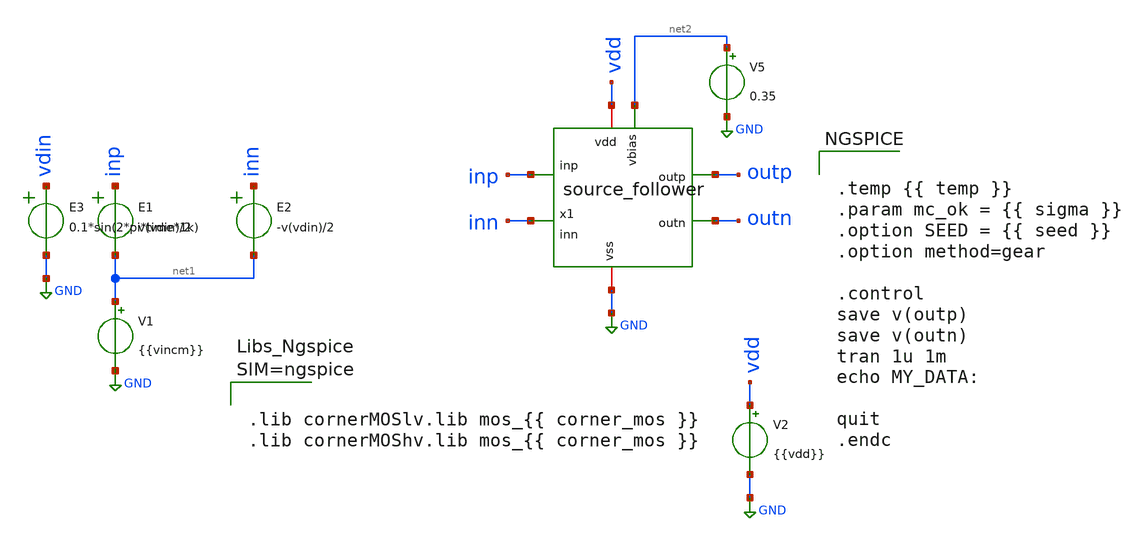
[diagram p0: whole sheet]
** sch_path: examples/source_follower/tb/tb_sf_tran.sch
**.subckt tb_sf_tran
E1 inp net1 VOL=' v(vdin)/2 '
E2 inn net1 VOL=' -v(vdin)/2 '
V1 net1 GND {{vincm}}
.save i(v1)
V2 vdd GND {{vdd}}
V5 net2 GND 0.35
.save i(v5)
x1 vdd inn inp outp outn net2 GND source_follower
E3 vdin GND VOL=' 0.1*sin(2*pi*time*1k) '
**** begin user architecture code


.temp {{ temp }}
.param mc_ok = {{ sigma }}
.option SEED = {{ seed }}
.option method=gear

.control
save v(outp)
save v(outn)
tran 1u 1m
echo MY_DATA:

quit
.endc





.lib cornerMOSlv.lib mos_{{ corner_mos }}
.lib cornerMOShv.lib mos_{{ corner_mos }}



**** end user architecture code
**.ends

* expanding   symbol:  chipify/examples/source_follower/sch/source_follower.sym # of pins=7
** sym_path: examples/source_follower/sch/source_follower.sym
** sch_path: examples/source_follower/sch/source_follower.sch
.subckt source_follower vdd inn inp outp outn vbias vss
*.ipin vbias
*.iopin vdd
*.opin outp
*.iopin vss
*.opin outn
*.ipin inp
*.ipin inn
XM1 outp vbias vss vss sg13_lv_nmos w=100u l=2u ng=20 m=1 mm_ok=1
XM2 vdd inp outp vss sg13_lv_nmos w=200u l=0.13u ng=20 m=1 mm_ok=1
XM3 outn vbias vss vss sg13_lv_nmos w=100u l=2u ng=20 m=1 mm_ok=1
XM4 vdd inn outn vss sg13_lv_nmos w=200u l=0.13u ng=20 m=1 mm_ok=1
.ends

.GLOBAL GND
.end
